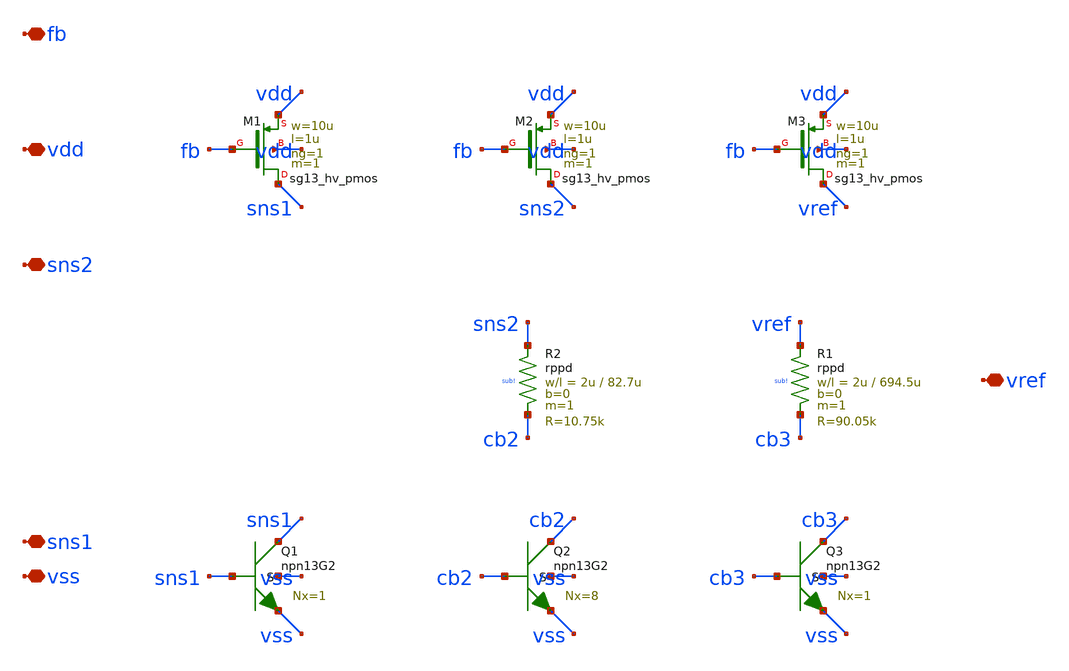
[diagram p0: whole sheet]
** sch_path: design/bandgap_core.sch
**.subckt bandgap_core vdd vss fb sns1 sns2 vref
*.iopin vdd
*.iopin vss
*.iopin fb
*.iopin sns1
*.iopin sns2
*.iopin vref
XM1 sns1 fb vdd vdd sg13_hv_pmos w=10u l=1u ng=1 m=1 mm_ok=1
XQ1 sns1 sns1 vss vss npn13G2 Nx=1 mm_ok=1
XM2 sns2 fb vdd vdd sg13_hv_pmos w=10u l=1u ng=1 m=1 mm_ok=1
XR2 sns2 cb2 sub! rppd w=2u l=82.7u m=1 b=0 mm_ok=1
XQ2 cb2 cb2 vss vss npn13G2 Nx=8 mm_ok=1
XM3 vref fb vdd vdd sg13_hv_pmos w=10u l=1u ng=1 m=1 mm_ok=1
XR1 vref cb3 sub! rppd w=2u l=694.5u m=1 b=0 mm_ok=1
XQ3 cb3 cb3 vss vss npn13G2 Nx=1 mm_ok=1
**.ends
.end
